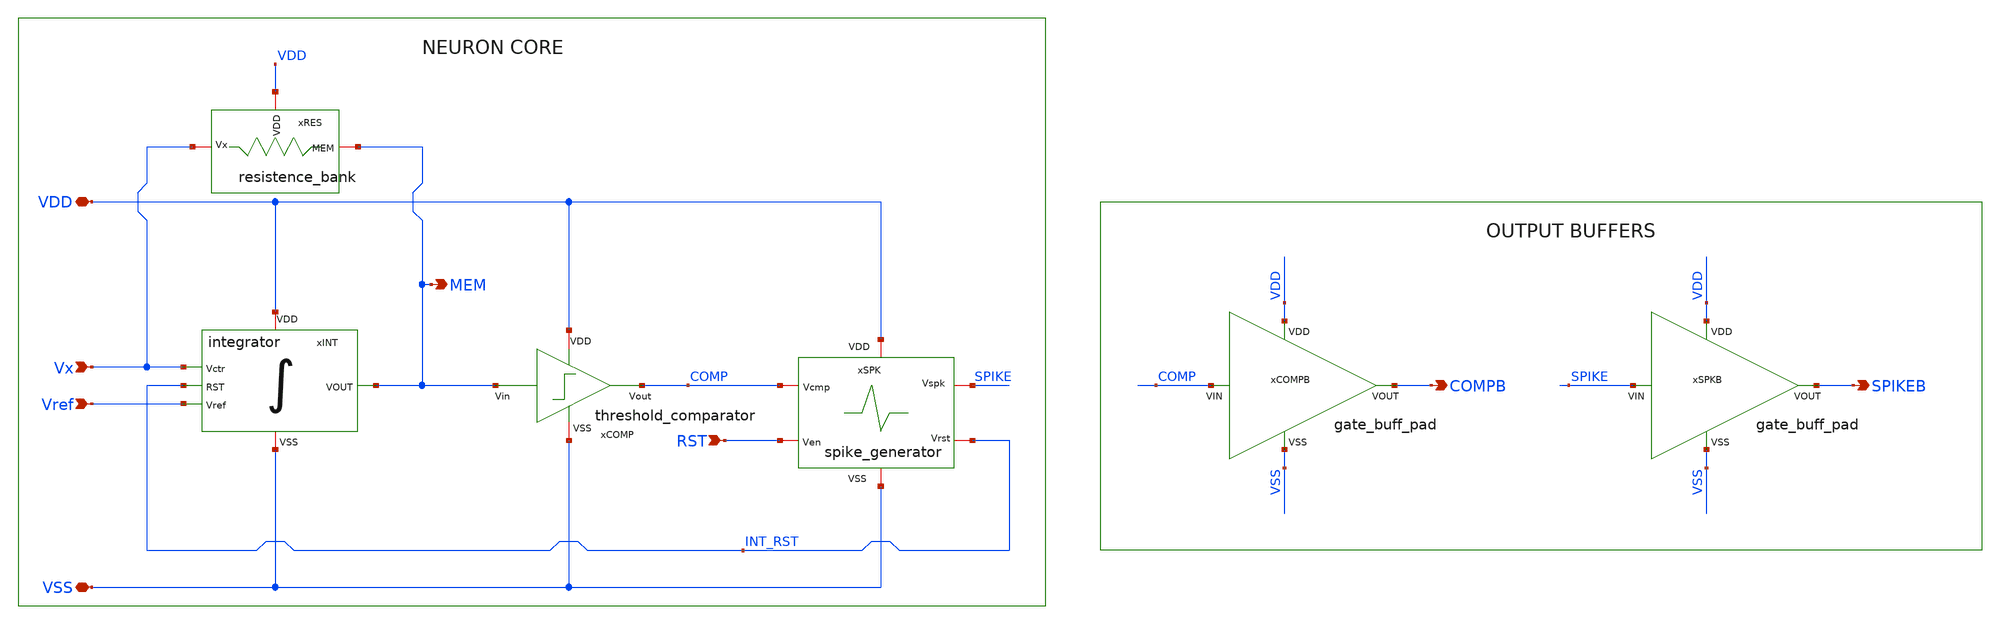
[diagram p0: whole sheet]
** sch_path: OSC9996-main/schematic/xschem/TOP_ROILIFNEURON.sch
**.subckt TOP_ROILIFNEURON VDD VSS MEM Vx Vref SPIKEB RST COMPB
*.iopin VDD
*.iopin VSS
*.opin MEM
*.ipin Vx
*.ipin Vref
*.opin SPIKEB
*.ipin RST
*.opin COMPB
xINT Vref VSS VDD INT_RST Vx MEM integrator
xSPK VDD COMP SPIKE INT_RST RST VSS spike_generator
xRES VDD MEM Vx resistence_bank
xCOMP VDD MEM COMP VSS threshold_comparator
xSPKB VDD SPIKE SPIKEB VSS gate_buff_pad
xCOMPB VDD COMP COMPB VSS gate_buff_pad
**.ends
.end
